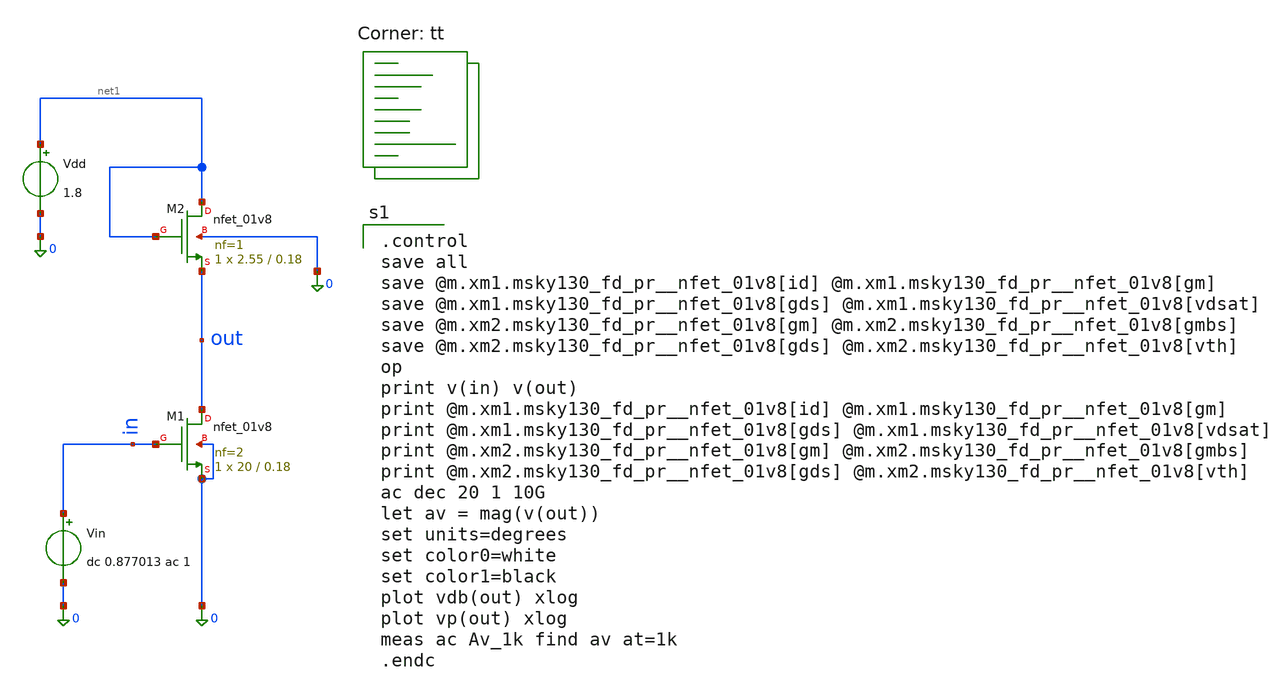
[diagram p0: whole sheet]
** sch_path: Homework 4 - Differential Pair Small Signal Gain/Simulations/ex6_final.sch
**.subckt ex6_final
Vin in 0 dc 0.877013 ac 1
XM1 out in 0 0 sky130_fd_pr__nfet_01v8 L=0.18 W=20 nf=2 ad='int((2 + 1)/2) * 20 / 2 * 0.29' as='int((2 + 2)/2) * 20 / 2 * 0.29'
+ pd='2*int((2 + 1)/2) * (20 / 2 + 0.29)' ps='2*int((2 + 2)/2) * (20 / 2 + 0.29)' nrd='0.29 / 20 ' nrs='0.29 / 20 '
+ sa=0 sb=0 sd=0 mult=1 m=1
Vdd net1 0 1.8
XM2 net1 net1 out 0 sky130_fd_pr__nfet_01v8 L=0.18 W=2.55 nf=1 ad='int((1 + 1)/2) * 2.55 / 1 * 0.29'
+ as='int((1 + 2)/2) * 2.55 / 1 * 0.29' pd='2*int((1 + 1)/2) * (2.55 / 1 + 0.29)' ps='2*int((1 + 2)/2) * (2.55 / 1 + 0.29)'
+ nrd='0.29 / 2.55 ' nrs='0.29 / 2.55 ' sa=0 sb=0 sd=0 mult=1 m=1
**** begin user architecture code
.lib $::SKYWATER_MODELS/sky130.lib.spice tt

.control
save all
save @m.xm1.msky130_fd_pr__nfet_01v8[id] @m.xm1.msky130_fd_pr__nfet_01v8[gm]
save @m.xm1.msky130_fd_pr__nfet_01v8[gds] @m.xm1.msky130_fd_pr__nfet_01v8[vdsat]
save @m.xm2.msky130_fd_pr__nfet_01v8[gm] @m.xm2.msky130_fd_pr__nfet_01v8[gmbs]
save @m.xm2.msky130_fd_pr__nfet_01v8[gds] @m.xm2.msky130_fd_pr__nfet_01v8[vth]
op
print v(in) v(out)
print @m.xm1.msky130_fd_pr__nfet_01v8[id] @m.xm1.msky130_fd_pr__nfet_01v8[gm]
print @m.xm1.msky130_fd_pr__nfet_01v8[gds] @m.xm1.msky130_fd_pr__nfet_01v8[vdsat]
print @m.xm2.msky130_fd_pr__nfet_01v8[gm] @m.xm2.msky130_fd_pr__nfet_01v8[gmbs]
print @m.xm2.msky130_fd_pr__nfet_01v8[gds] @m.xm2.msky130_fd_pr__nfet_01v8[vth]
ac dec 20 1 10G
let av = mag(v(out))
set units=degrees
set color0=white
set color1=black
plot vdb(out) xlog
plot vp(out) xlog
meas ac Av_1k find av at=1k
.endc


**** end user architecture code
**.ends
.end
